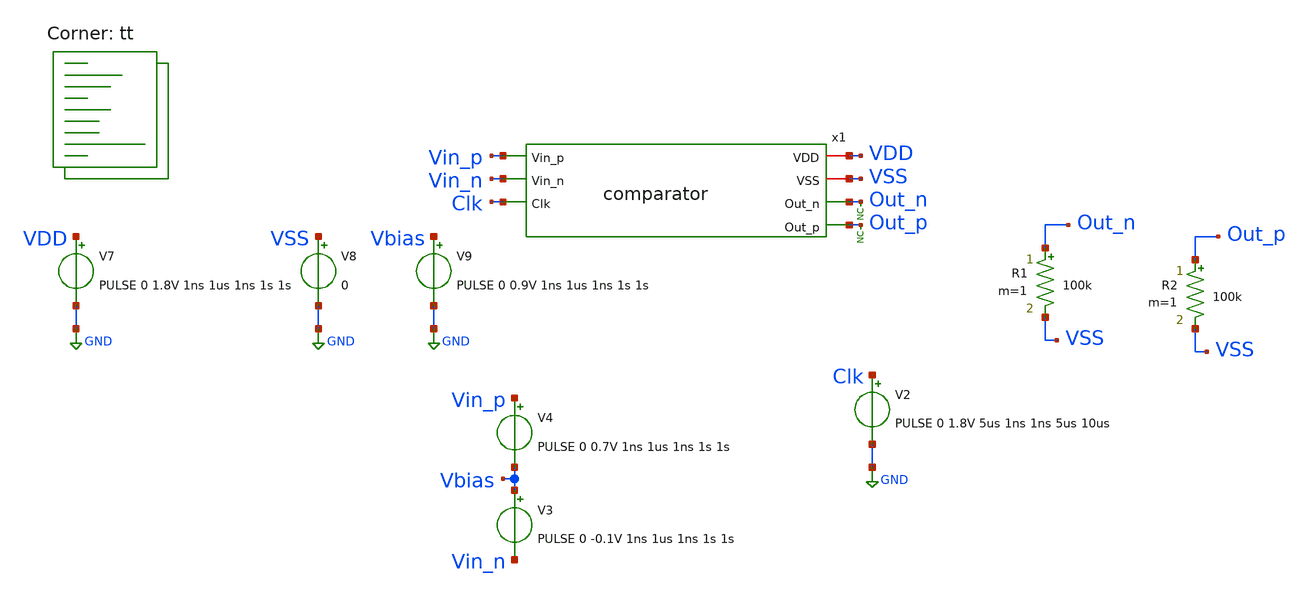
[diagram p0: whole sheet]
** sch_path: xschem/tests/comparator/comparator_power_ramp_in_test.sch
**.subckt comparator_power_ramp_in_test
x1 VDD VSS Vin_p Out_n Vin_n Out_p Clk comparator
V2 Clk GND PULSE 0 1.8V 5us 1ns 1ns 5us 10us
* noconn Out_p
* noconn Out_n
R1 Out_n VSS 100k m=1
R2 Out_p VSS 100k m=1
V7 VDD GND PULSE 0 1.8V 1ns 1us 1ns 1s 1s
V8 VSS GND 0
V9 Vbias GND PULSE 0 0.9V 1ns 1us 1ns 1s 1s
V3 Vbias Vin_n PULSE 0 -0.1V 1ns 1us 1ns 1s 1s
V4 Vin_p Vbias PULSE 0 0.7V 1ns 1us 1ns 1s 1s
**** begin user architecture code
 *.lib $::SKYWATER_MODELS/sky130.lib.spice tt
.include $::SKYWATER_STDCELLS/sky130_fd_sc_hd.spice


.options acct list
.temp 25
*vvcc VDD 0 dc 1.8
*vvss VSS 0 0
.control
save all
tran 0.1u 200u uic
*dc V1 0 1.8V 0.1
plot Vin_p-Vin_n Out_p-Out_n Clk-4
plot Vin_p-Vin_n x1.pre_amp_p-x1.pre_amp_n Clk-4
plot Vin_p Vin_n x1.pre_amp_p+2 x1.pre_amp_n+2 Clk-4
write comparator_test.raw
.endc


.lib $::SKYWATER_MODELS/sky130.lib.spice tt
**** end user architecture code
**.ends

* expanding   symbol:  src/comparator/comparator.sym # of pins=7
** sym_path: xschem/src/comparator/comparator.sym
** sch_path: xschem/src/comparator/comparator.sch
.subckt comparator VDD VSS Vin_p Out_n Vin_n Out_p Clk
*.iopin VDD
*.iopin VSS
*.ipin Vin_p
*.opin Out_n
*.ipin Vin_n
*.opin Out_p
*.ipin Clk
XM1 Pre_Amp_n Clk VDD VSS sky130_fd_pr__pfet_01v8 L=0.15 W=1 nf=1 ad='int((nf+1)/2) * W/nf * 0.29' as='int((nf+2)/2) * W/nf * 0.29'
+ pd='2*int((nf+1)/2) * (W/nf + 0.29)' ps='2*int((nf+2)/2) * (W/nf + 0.29)' nrd='0.29 / W' nrs='0.29 / W'
+ sa=0 sb=0 sd=0 mult=1 m=1
XM2 Pre_Amp_p Clk VDD VSS sky130_fd_pr__pfet_01v8 L=0.15 W=1 nf=1 ad='int((nf+1)/2) * W/nf * 0.29' as='int((nf+2)/2) * W/nf * 0.29'
+ pd='2*int((nf+1)/2) * (W/nf + 0.29)' ps='2*int((nf+2)/2) * (W/nf + 0.29)' nrd='0.29 / W' nrs='0.29 / W'
+ sa=0 sb=0 sd=0 mult=1 m=1
XM3 Pre_Amp_p Vin_p net1 VSS sky130_fd_pr__nfet_01v8 L=0.15 W=1 nf=1 ad='int((nf+1)/2) * W/nf * 0.29'
+ as='int((nf+2)/2) * W/nf * 0.29' pd='2*int((nf+1)/2) * (W/nf + 0.29)' ps='2*int((nf+2)/2) * (W/nf + 0.29)'
+ nrd='0.29 / W' nrs='0.29 / W' sa=0 sb=0 sd=0 mult=1 m=1
XM4 Pre_Amp_n Vin_n net1 VSS sky130_fd_pr__nfet_01v8 L=0.15 W=1 nf=1 ad='int((nf+1)/2) * W/nf * 0.29'
+ as='int((nf+2)/2) * W/nf * 0.29' pd='2*int((nf+1)/2) * (W/nf + 0.29)' ps='2*int((nf+2)/2) * (W/nf + 0.29)'
+ nrd='0.29 / W' nrs='0.29 / W' sa=0 sb=0 sd=0 mult=1 m=1
XM5 net3 Out_p VDD VSS sky130_fd_pr__pfet_01v8 L=0.15 W=1 nf=1 ad='int((nf+1)/2) * W/nf * 0.29' as='int((nf+2)/2) * W/nf * 0.29'
+ pd='2*int((nf+1)/2) * (W/nf + 0.29)' ps='2*int((nf+2)/2) * (W/nf + 0.29)' nrd='0.29 / W' nrs='0.29 / W'
+ sa=0 sb=0 sd=0 mult=1 m=1
XM6 net2 Out_n VDD VSS sky130_fd_pr__pfet_01v8 L=0.15 W=1 nf=1 ad='int((nf+1)/2) * W/nf * 0.29' as='int((nf+2)/2) * W/nf * 0.29'
+ pd='2*int((nf+1)/2) * (W/nf + 0.29)' ps='2*int((nf+2)/2) * (W/nf + 0.29)' nrd='0.29 / W' nrs='0.29 / W'
+ sa=0 sb=0 sd=0 mult=1 m=1
XM7 net2 Pre_Amp_p Out_p VSS sky130_fd_pr__nfet_01v8 L=0.15 W=1 nf=1 ad='int((nf+1)/2) * W/nf * 0.29'
+ as='int((nf+2)/2) * W/nf * 0.29' pd='2*int((nf+1)/2) * (W/nf + 0.29)' ps='2*int((nf+2)/2) * (W/nf + 0.29)'
+ nrd='0.29 / W' nrs='0.29 / W' sa=0 sb=0 sd=0 mult=1 m=1
XM8 net3 Pre_Amp_n Out_n VSS sky130_fd_pr__nfet_01v8 L=0.15 W=1 nf=1 ad='int((nf+1)/2) * W/nf * 0.29'
+ as='int((nf+2)/2) * W/nf * 0.29' pd='2*int((nf+1)/2) * (W/nf + 0.29)' ps='2*int((nf+2)/2) * (W/nf + 0.29)'
+ nrd='0.29 / W' nrs='0.29 / W' sa=0 sb=0 sd=0 mult=1 m=1
XM9 net1 Clk VSS VSS sky130_fd_pr__nfet_01v8 L=0.15 W=1 nf=1 ad='int((nf+1)/2) * W/nf * 0.29' as='int((nf+2)/2) * W/nf * 0.29'
+ pd='2*int((nf+1)/2) * (W/nf + 0.29)' ps='2*int((nf+2)/2) * (W/nf + 0.29)' nrd='0.29 / W' nrs='0.29 / W'
+ sa=0 sb=0 sd=0 mult=1 m=1
XM10 Pre_Amp_n Vin_n net1 VSS sky130_fd_pr__nfet_01v8 L=0.15 W=1 nf=1 ad='int((nf+1)/2) * W/nf * 0.29'
+ as='int((nf+2)/2) * W/nf * 0.29' pd='2*int((nf+1)/2) * (W/nf + 0.29)' ps='2*int((nf+2)/2) * (W/nf + 0.29)'
+ nrd='0.29 / W' nrs='0.29 / W' sa=0 sb=0 sd=0 mult=1 m=1
XM11 Out_n Clk_n VSS VSS sky130_fd_pr__nfet_01v8 L=0.15 W=1 nf=1 ad='int((nf+1)/2) * W/nf * 0.29' as='int((nf+2)/2) * W/nf * 0.29'
+ pd='2*int((nf+1)/2) * (W/nf + 0.29)' ps='2*int((nf+2)/2) * (W/nf + 0.29)' nrd='0.29 / W' nrs='0.29 / W'
+ sa=0 sb=0 sd=0 mult=1 m=1
XM12 Out_n Out_p VSS VSS sky130_fd_pr__nfet_01v8 L=0.15 W=1 nf=1 ad='int((nf+1)/2) * W/nf * 0.29' as='int((nf+2)/2) * W/nf * 0.29'
+ pd='2*int((nf+1)/2) * (W/nf + 0.29)' ps='2*int((nf+2)/2) * (W/nf + 0.29)' nrd='0.29 / W' nrs='0.29 / W'
+ sa=0 sb=0 sd=0 mult=1 m=1
XM13 Out_p Out_n VSS VSS sky130_fd_pr__nfet_01v8 L=0.15 W=1 nf=1 ad='int((nf+1)/2) * W/nf * 0.29' as='int((nf+2)/2) * W/nf * 0.29'
+ pd='2*int((nf+1)/2) * (W/nf + 0.29)' ps='2*int((nf+2)/2) * (W/nf + 0.29)' nrd='0.29 / W' nrs='0.29 / W'
+ sa=0 sb=0 sd=0 mult=1 m=1
XM14 Out_p Clk_n VSS VSS sky130_fd_pr__nfet_01v8 L=0.15 W=1 nf=1 ad='int((nf+1)/2) * W/nf * 0.29' as='int((nf+2)/2) * W/nf * 0.29'
+ pd='2*int((nf+1)/2) * (W/nf + 0.29)' ps='2*int((nf+2)/2) * (W/nf + 0.29)' nrd='0.29 / W' nrs='0.29 / W'
+ sa=0 sb=0 sd=0 mult=1 m=1
XM15 Clk_n Clk VDD VSS sky130_fd_pr__pfet_01v8 L=0.15 W=1 nf=1 ad='int((nf+1)/2) * W/nf * 0.29' as='int((nf+2)/2) * W/nf * 0.29'
+ pd='2*int((nf+1)/2) * (W/nf + 0.29)' ps='2*int((nf+2)/2) * (W/nf + 0.29)' nrd='0.29 / W' nrs='0.29 / W'
+ sa=0 sb=0 sd=0 mult=1 m=1
XM16 Clk_n Clk VSS VSS sky130_fd_pr__nfet_01v8 L=0.15 W=1 nf=1 ad='int((nf+1)/2) * W/nf * 0.29' as='int((nf+2)/2) * W/nf * 0.29'
+ pd='2*int((nf+1)/2) * (W/nf + 0.29)' ps='2*int((nf+2)/2) * (W/nf + 0.29)' nrd='0.29 / W' nrs='0.29 / W'
+ sa=0 sb=0 sd=0 mult=1 m=1
.ends

.GLOBAL GND
.end
